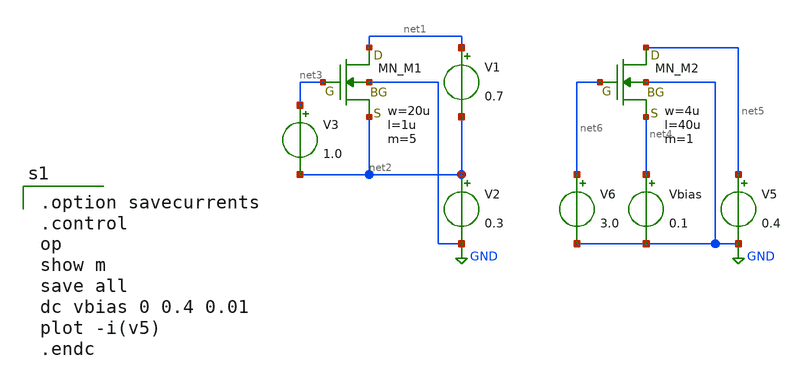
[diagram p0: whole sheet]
** sch_path: member_project/DCDC/ShuntaroOHNO/xschem/nmos_id_bias.sch
**.subckt nmos_id_bias
V1 net1 net2 0.7
XM1 net1 net3 net2 GND NMOS w=20u l=1u as=0 ad=0 ps=0 pd=0 nrd=0 nrs=0 m=5
V2 net2 GND 0.3
V3 net3 net2 1.0
XM2 net5 net6 net4 GND NMOS w=4u l=40u as=0 ad=0 ps=0 pd=0 nrd=0 nrs=0 m=1
V5 net5 GND 0.4
V6 net6 GND 3.0
Vbias net4 GND 0.1
**** begin user architecture code
 .include $::LIB/ip62_models

.option savecurrents
.control
op
show m
save all
dc vbias 0 0.4 0.01
plot -i(v5)
.endc

**** end user architecture code
**.ends
.GLOBAL GND
.end
